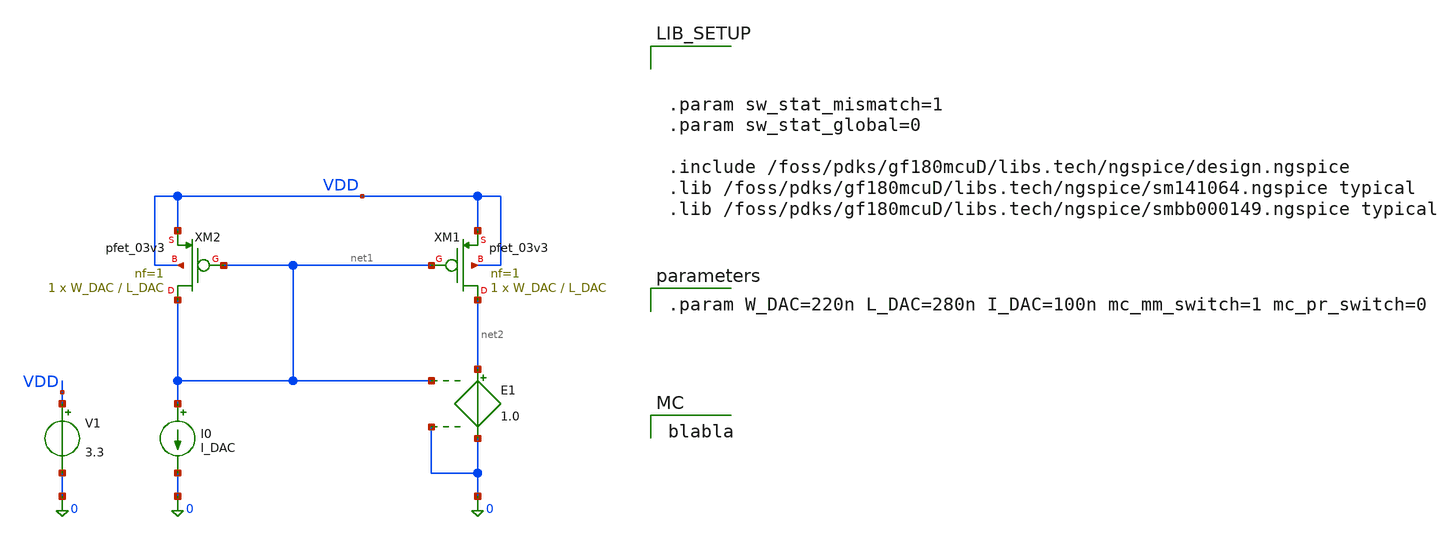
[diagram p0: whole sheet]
** sch_path: lab_2/lab2.sch
**.subckt lab2
I0 net1 0 I_DAC
E1 net2 0 net1 0 1.0
V1 VDD 0 3.3
XM1 net2 net1 VDD VDD pfet_03v3 L=L_DAC W=W_DAC nf=1 ad='int((nf+1)/2) * W/nf * 0.18u' as='int((nf+2)/2) * W/nf * 0.18u'
+ pd='2*int((nf+1)/2) * (W/nf + 0.18u)' ps='2*int((nf+2)/2) * (W/nf + 0.18u)' nrd='0.18u / W' nrs='0.18u / W'
+ sa=0 sb=0 sd=0 m=1
XM2 net1 net1 VDD VDD pfet_03v3 L=L_DAC W=W_DAC nf=1 ad='int((nf+1)/2) * W/nf * 0.18u' as='int((nf+2)/2) * W/nf * 0.18u'
+ pd='2*int((nf+1)/2) * (W/nf + 0.18u)' ps='2*int((nf+2)/2) * (W/nf + 0.18u)' nrd='0.18u / W' nrs='0.18u / W'
+ sa=0 sb=0 sd=0 m=1
**** begin user architecture code



.param sw_stat_mismatch=1
.param sw_stat_global=0

.include /foss/pdks/gf180mcuD/libs.tech/ngspice/design.ngspice
.lib /foss/pdks/gf180mcuD/libs.tech/ngspice/sm141064.ngspice typical
.lib /foss/pdks/gf180mcuD/libs.tech/ngspice/smbb000149.ngspice typical



.param W_DAC=220n L_DAC=280n I_DAC=100n mc_mm_switch=1 mc_pr_switch=0



blabla

**** end user architecture code
**.ends
.end
